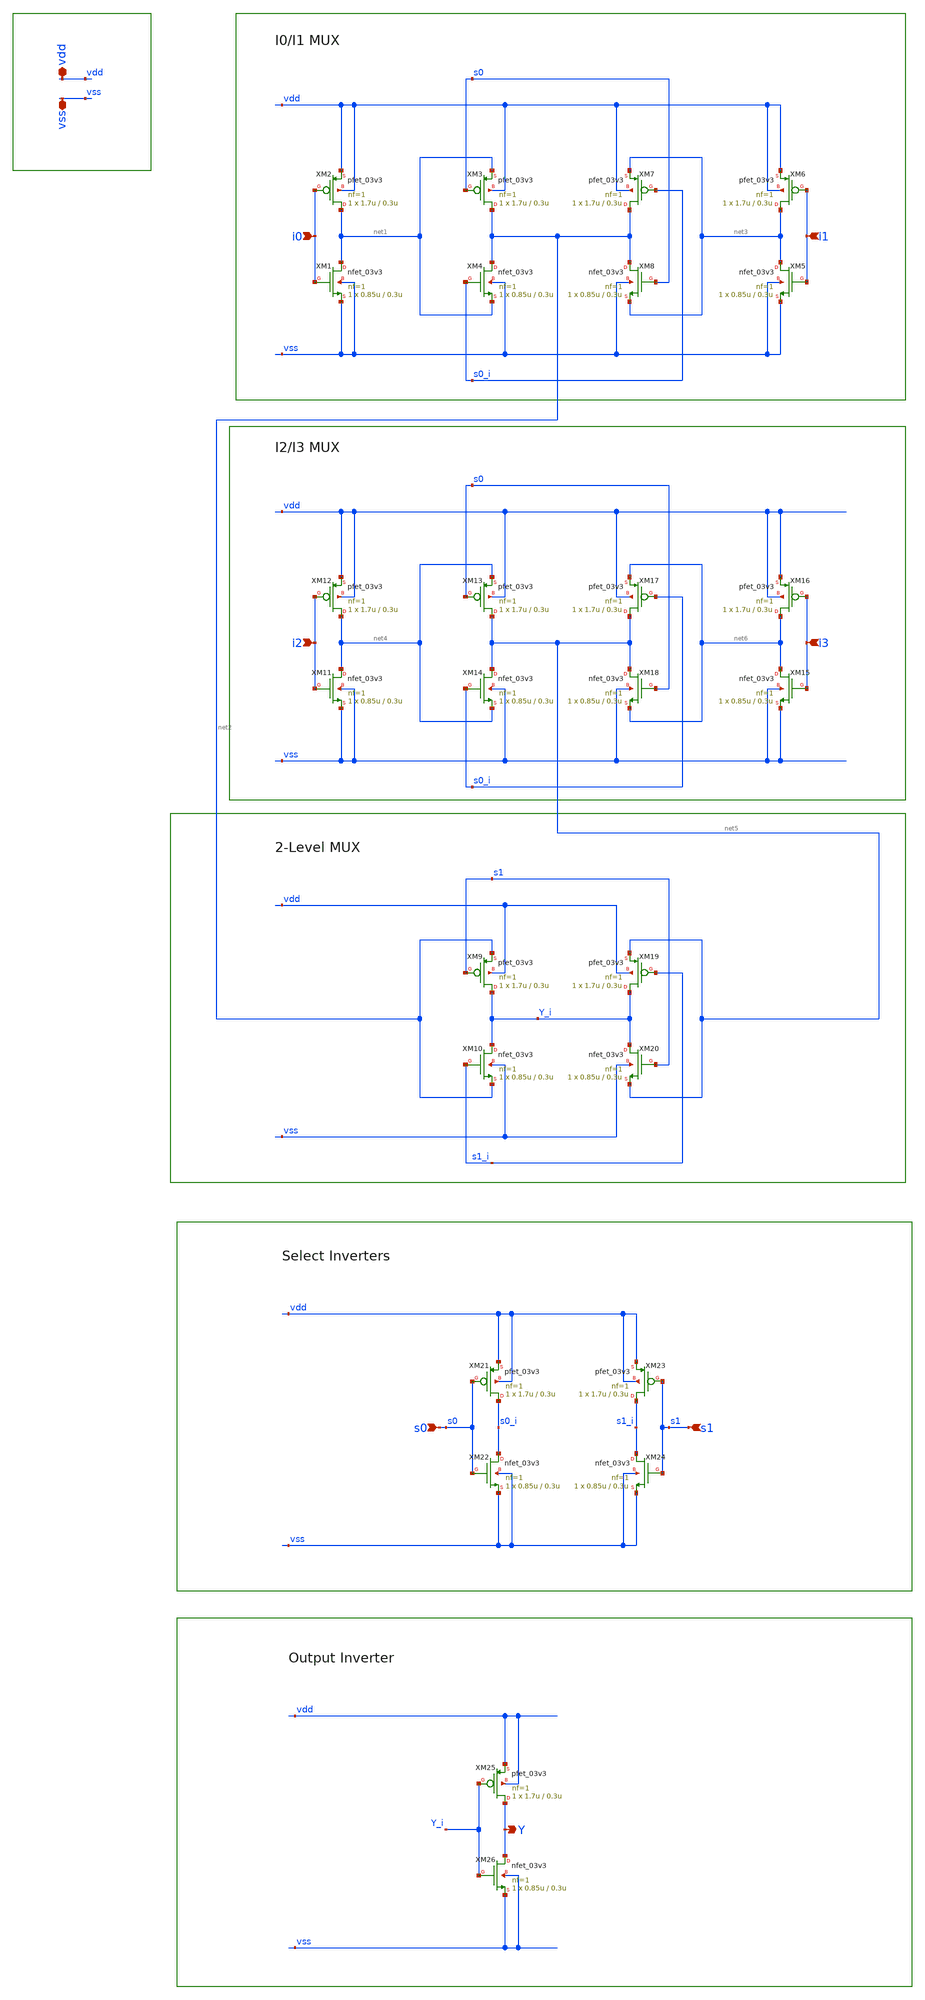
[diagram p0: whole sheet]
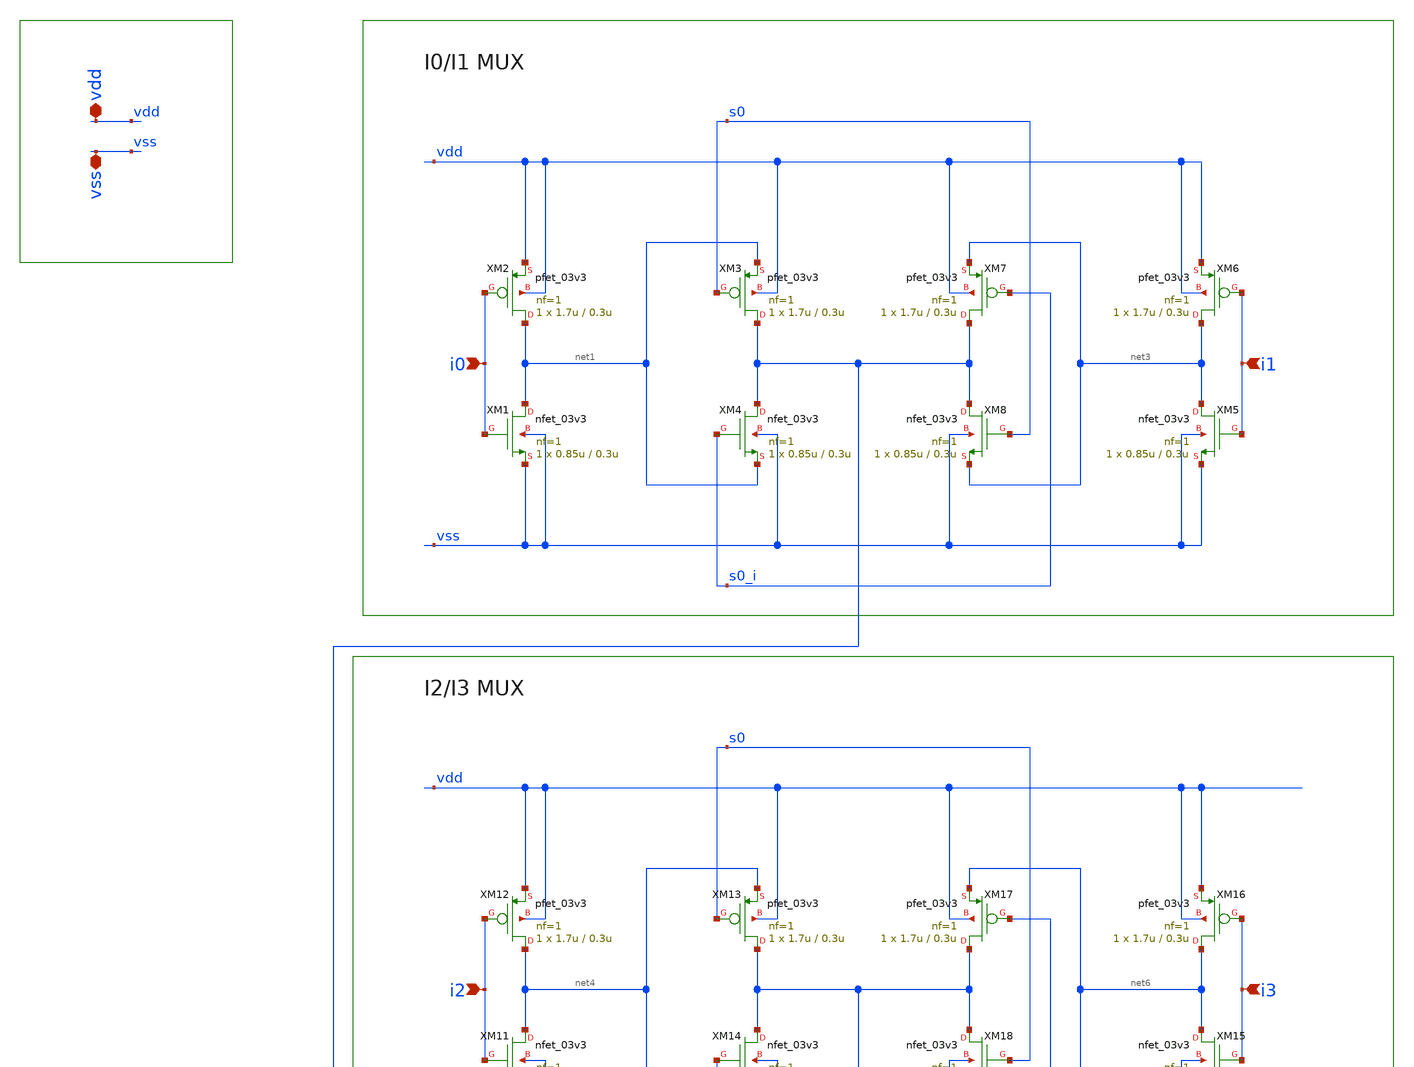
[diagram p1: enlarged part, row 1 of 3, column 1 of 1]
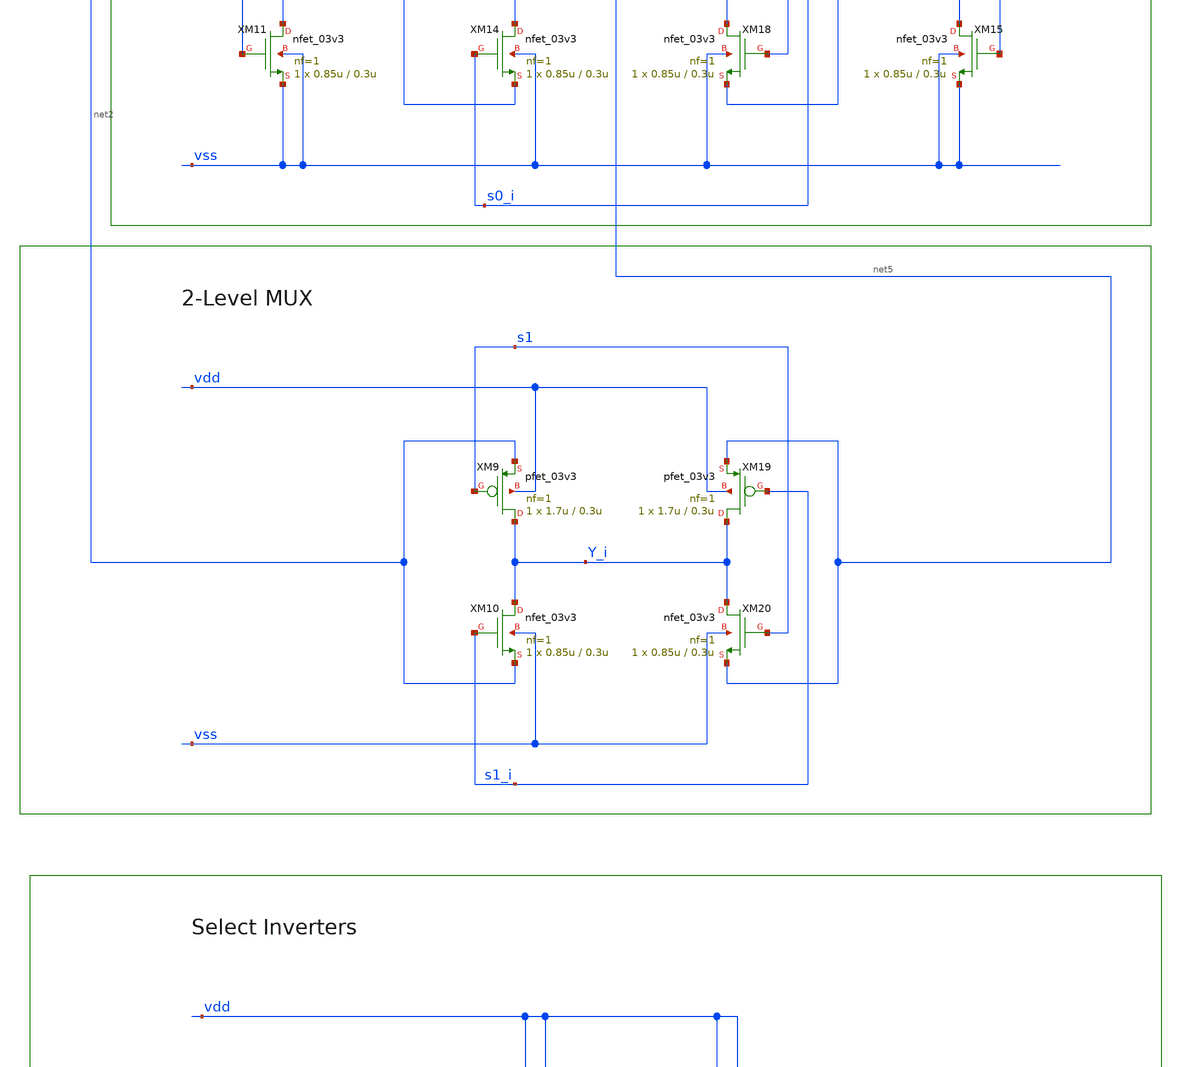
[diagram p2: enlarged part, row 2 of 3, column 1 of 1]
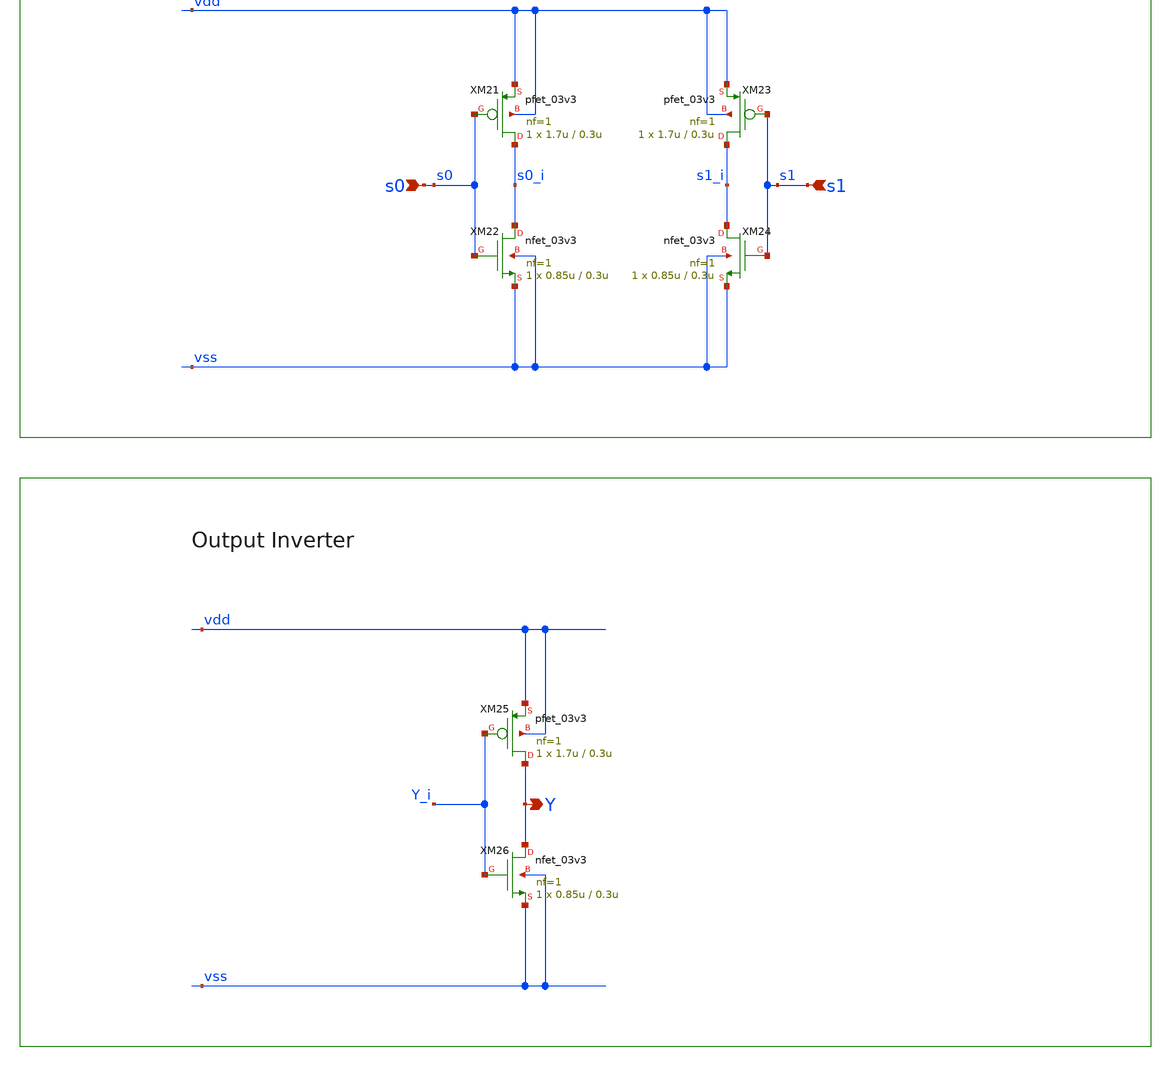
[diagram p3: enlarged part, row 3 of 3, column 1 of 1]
** sch_path: yuri-preliminary-work/mux4.sch
**.subckt mux4 vss vdd i0 i1 i2 i3 s0 s1 Y
*.iopin vss
*.iopin vdd
*.ipin i0
*.ipin i1
*.ipin i2
*.ipin i3
*.ipin s0
*.ipin s1
*.opin Y
XM1 net1 i0 vss vss nfet_03v3 L=0.3u W=0.85u nf=1 ad='int((nf+1)/2) * W/nf * 0.18u' as='int((nf+2)/2) * W/nf * 0.18u'
+ pd='2*int((nf+1)/2) * (W/nf + 0.18u)' ps='2*int((nf+2)/2) * (W/nf + 0.18u)' nrd='0.18u / W' nrs='0.18u / W'
+ sa=0 sb=0 sd=0 m=1
XM2 net1 i0 vdd vdd pfet_03v3 L=0.3u W=1.7u nf=1 ad='int((nf+1)/2) * W/nf * 0.18u' as='int((nf+2)/2) * W/nf * 0.18u'
+ pd='2*int((nf+1)/2) * (W/nf + 0.18u)' ps='2*int((nf+2)/2) * (W/nf + 0.18u)' nrd='0.18u / W' nrs='0.18u / W'
+ sa=0 sb=0 sd=0 m=1
XM3 net2 s0 net1 vdd pfet_03v3 L=0.3u W=1.7u nf=1 ad='int((nf+1)/2) * W/nf * 0.18u' as='int((nf+2)/2) * W/nf * 0.18u'
+ pd='2*int((nf+1)/2) * (W/nf + 0.18u)' ps='2*int((nf+2)/2) * (W/nf + 0.18u)' nrd='0.18u / W' nrs='0.18u / W'
+ sa=0 sb=0 sd=0 m=1
XM4 net2 s0_i net1 vss nfet_03v3 L=0.3u W=0.85u nf=1 ad='int((nf+1)/2) * W/nf * 0.18u' as='int((nf+2)/2) * W/nf * 0.18u'
+ pd='2*int((nf+1)/2) * (W/nf + 0.18u)' ps='2*int((nf+2)/2) * (W/nf + 0.18u)' nrd='0.18u / W' nrs='0.18u / W'
+ sa=0 sb=0 sd=0 m=1
XM5 net3 i1 vss vss nfet_03v3 L=0.3u W=0.85u nf=1 ad='int((nf+1)/2) * W/nf * 0.18u' as='int((nf+2)/2) * W/nf * 0.18u'
+ pd='2*int((nf+1)/2) * (W/nf + 0.18u)' ps='2*int((nf+2)/2) * (W/nf + 0.18u)' nrd='0.18u / W' nrs='0.18u / W'
+ sa=0 sb=0 sd=0 m=1
XM6 net3 i1 vdd vdd pfet_03v3 L=0.3u W=1.7u nf=1 ad='int((nf+1)/2) * W/nf * 0.18u' as='int((nf+2)/2) * W/nf * 0.18u'
+ pd='2*int((nf+1)/2) * (W/nf + 0.18u)' ps='2*int((nf+2)/2) * (W/nf + 0.18u)' nrd='0.18u / W' nrs='0.18u / W'
+ sa=0 sb=0 sd=0 m=1
XM7 net2 s0_i net3 vdd pfet_03v3 L=0.3u W=1.7u nf=1 ad='int((nf+1)/2) * W/nf * 0.18u' as='int((nf+2)/2) * W/nf * 0.18u'
+ pd='2*int((nf+1)/2) * (W/nf + 0.18u)' ps='2*int((nf+2)/2) * (W/nf + 0.18u)' nrd='0.18u / W' nrs='0.18u / W'
+ sa=0 sb=0 sd=0 m=1
XM8 net2 s0 net3 vss nfet_03v3 L=0.3u W=0.85u nf=1 ad='int((nf+1)/2) * W/nf * 0.18u' as='int((nf+2)/2) * W/nf * 0.18u'
+ pd='2*int((nf+1)/2) * (W/nf + 0.18u)' ps='2*int((nf+2)/2) * (W/nf + 0.18u)' nrd='0.18u / W' nrs='0.18u / W'
+ sa=0 sb=0 sd=0 m=1
XM11 net4 i2 vss vss nfet_03v3 L=0.3u W=0.85u nf=1 ad='int((nf+1)/2) * W/nf * 0.18u' as='int((nf+2)/2) * W/nf * 0.18u'
+ pd='2*int((nf+1)/2) * (W/nf + 0.18u)' ps='2*int((nf+2)/2) * (W/nf + 0.18u)' nrd='0.18u / W' nrs='0.18u / W'
+ sa=0 sb=0 sd=0 m=1
XM12 net4 i2 vdd vdd pfet_03v3 L=0.3u W=1.7u nf=1 ad='int((nf+1)/2) * W/nf * 0.18u' as='int((nf+2)/2) * W/nf * 0.18u'
+ pd='2*int((nf+1)/2) * (W/nf + 0.18u)' ps='2*int((nf+2)/2) * (W/nf + 0.18u)' nrd='0.18u / W' nrs='0.18u / W'
+ sa=0 sb=0 sd=0 m=1
XM13 net5 s0 net4 vdd pfet_03v3 L=0.3u W=1.7u nf=1 ad='int((nf+1)/2) * W/nf * 0.18u' as='int((nf+2)/2) * W/nf * 0.18u'
+ pd='2*int((nf+1)/2) * (W/nf + 0.18u)' ps='2*int((nf+2)/2) * (W/nf + 0.18u)' nrd='0.18u / W' nrs='0.18u / W'
+ sa=0 sb=0 sd=0 m=1
XM14 net5 s0_i net4 vss nfet_03v3 L=0.3u W=0.85u nf=1 ad='int((nf+1)/2) * W/nf * 0.18u' as='int((nf+2)/2) * W/nf * 0.18u'
+ pd='2*int((nf+1)/2) * (W/nf + 0.18u)' ps='2*int((nf+2)/2) * (W/nf + 0.18u)' nrd='0.18u / W' nrs='0.18u / W'
+ sa=0 sb=0 sd=0 m=1
XM15 net6 i3 vss vss nfet_03v3 L=0.3u W=0.85u nf=1 ad='int((nf+1)/2) * W/nf * 0.18u' as='int((nf+2)/2) * W/nf * 0.18u'
+ pd='2*int((nf+1)/2) * (W/nf + 0.18u)' ps='2*int((nf+2)/2) * (W/nf + 0.18u)' nrd='0.18u / W' nrs='0.18u / W'
+ sa=0 sb=0 sd=0 m=1
XM16 net6 i3 vdd vdd pfet_03v3 L=0.3u W=1.7u nf=1 ad='int((nf+1)/2) * W/nf * 0.18u' as='int((nf+2)/2) * W/nf * 0.18u'
+ pd='2*int((nf+1)/2) * (W/nf + 0.18u)' ps='2*int((nf+2)/2) * (W/nf + 0.18u)' nrd='0.18u / W' nrs='0.18u / W'
+ sa=0 sb=0 sd=0 m=1
XM17 net5 s0_i net6 vdd pfet_03v3 L=0.3u W=1.7u nf=1 ad='int((nf+1)/2) * W/nf * 0.18u' as='int((nf+2)/2) * W/nf * 0.18u'
+ pd='2*int((nf+1)/2) * (W/nf + 0.18u)' ps='2*int((nf+2)/2) * (W/nf + 0.18u)' nrd='0.18u / W' nrs='0.18u / W'
+ sa=0 sb=0 sd=0 m=1
XM18 net5 s0 net6 vss nfet_03v3 L=0.3u W=0.85u nf=1 ad='int((nf+1)/2) * W/nf * 0.18u' as='int((nf+2)/2) * W/nf * 0.18u'
+ pd='2*int((nf+1)/2) * (W/nf + 0.18u)' ps='2*int((nf+2)/2) * (W/nf + 0.18u)' nrd='0.18u / W' nrs='0.18u / W'
+ sa=0 sb=0 sd=0 m=1
XM9 Y_i s1 net2 vdd pfet_03v3 L=0.3u W=1.7u nf=1 ad='int((nf+1)/2) * W/nf * 0.18u' as='int((nf+2)/2) * W/nf * 0.18u'
+ pd='2*int((nf+1)/2) * (W/nf + 0.18u)' ps='2*int((nf+2)/2) * (W/nf + 0.18u)' nrd='0.18u / W' nrs='0.18u / W'
+ sa=0 sb=0 sd=0 m=1
XM10 Y_i s1_i net2 vss nfet_03v3 L=0.3u W=0.85u nf=1 ad='int((nf+1)/2) * W/nf * 0.18u' as='int((nf+2)/2) * W/nf * 0.18u'
+ pd='2*int((nf+1)/2) * (W/nf + 0.18u)' ps='2*int((nf+2)/2) * (W/nf + 0.18u)' nrd='0.18u / W' nrs='0.18u / W'
+ sa=0 sb=0 sd=0 m=1
XM19 Y_i s1_i net5 vdd pfet_03v3 L=0.3u W=1.7u nf=1 ad='int((nf+1)/2) * W/nf * 0.18u' as='int((nf+2)/2) * W/nf * 0.18u'
+ pd='2*int((nf+1)/2) * (W/nf + 0.18u)' ps='2*int((nf+2)/2) * (W/nf + 0.18u)' nrd='0.18u / W' nrs='0.18u / W'
+ sa=0 sb=0 sd=0 m=1
XM20 Y_i s1 net5 vss nfet_03v3 L=0.3u W=0.85u nf=1 ad='int((nf+1)/2) * W/nf * 0.18u' as='int((nf+2)/2) * W/nf * 0.18u'
+ pd='2*int((nf+1)/2) * (W/nf + 0.18u)' ps='2*int((nf+2)/2) * (W/nf + 0.18u)' nrd='0.18u / W' nrs='0.18u / W'
+ sa=0 sb=0 sd=0 m=1
XM21 s0_i s0 vdd vdd pfet_03v3 L=0.3u W=1.7u nf=1 ad='int((nf+1)/2) * W/nf * 0.18u' as='int((nf+2)/2) * W/nf * 0.18u'
+ pd='2*int((nf+1)/2) * (W/nf + 0.18u)' ps='2*int((nf+2)/2) * (W/nf + 0.18u)' nrd='0.18u / W' nrs='0.18u / W'
+ sa=0 sb=0 sd=0 m=1
XM22 s0_i s0 vss vss nfet_03v3 L=0.3u W=0.85u nf=1 ad='int((nf+1)/2) * W/nf * 0.18u' as='int((nf+2)/2) * W/nf * 0.18u'
+ pd='2*int((nf+1)/2) * (W/nf + 0.18u)' ps='2*int((nf+2)/2) * (W/nf + 0.18u)' nrd='0.18u / W' nrs='0.18u / W'
+ sa=0 sb=0 sd=0 m=1
XM23 s1_i s1 vdd vdd pfet_03v3 L=0.3u W=1.7u nf=1 ad='int((nf+1)/2) * W/nf * 0.18u' as='int((nf+2)/2) * W/nf * 0.18u'
+ pd='2*int((nf+1)/2) * (W/nf + 0.18u)' ps='2*int((nf+2)/2) * (W/nf + 0.18u)' nrd='0.18u / W' nrs='0.18u / W'
+ sa=0 sb=0 sd=0 m=1
XM24 s1_i s1 vss vss nfet_03v3 L=0.3u W=0.85u nf=1 ad='int((nf+1)/2) * W/nf * 0.18u' as='int((nf+2)/2) * W/nf * 0.18u'
+ pd='2*int((nf+1)/2) * (W/nf + 0.18u)' ps='2*int((nf+2)/2) * (W/nf + 0.18u)' nrd='0.18u / W' nrs='0.18u / W'
+ sa=0 sb=0 sd=0 m=1
XM25 Y Y_i vdd vdd pfet_03v3 L=0.3u W=1.7u nf=1 ad='int((nf+1)/2) * W/nf * 0.18u' as='int((nf+2)/2) * W/nf * 0.18u'
+ pd='2*int((nf+1)/2) * (W/nf + 0.18u)' ps='2*int((nf+2)/2) * (W/nf + 0.18u)' nrd='0.18u / W' nrs='0.18u / W'
+ sa=0 sb=0 sd=0 m=1
XM26 Y Y_i vss vss nfet_03v3 L=0.3u W=0.85u nf=1 ad='int((nf+1)/2) * W/nf * 0.18u' as='int((nf+2)/2) * W/nf * 0.18u'
+ pd='2*int((nf+1)/2) * (W/nf + 0.18u)' ps='2*int((nf+2)/2) * (W/nf + 0.18u)' nrd='0.18u / W' nrs='0.18u / W'
+ sa=0 sb=0 sd=0 m=1
**.ends
.end
